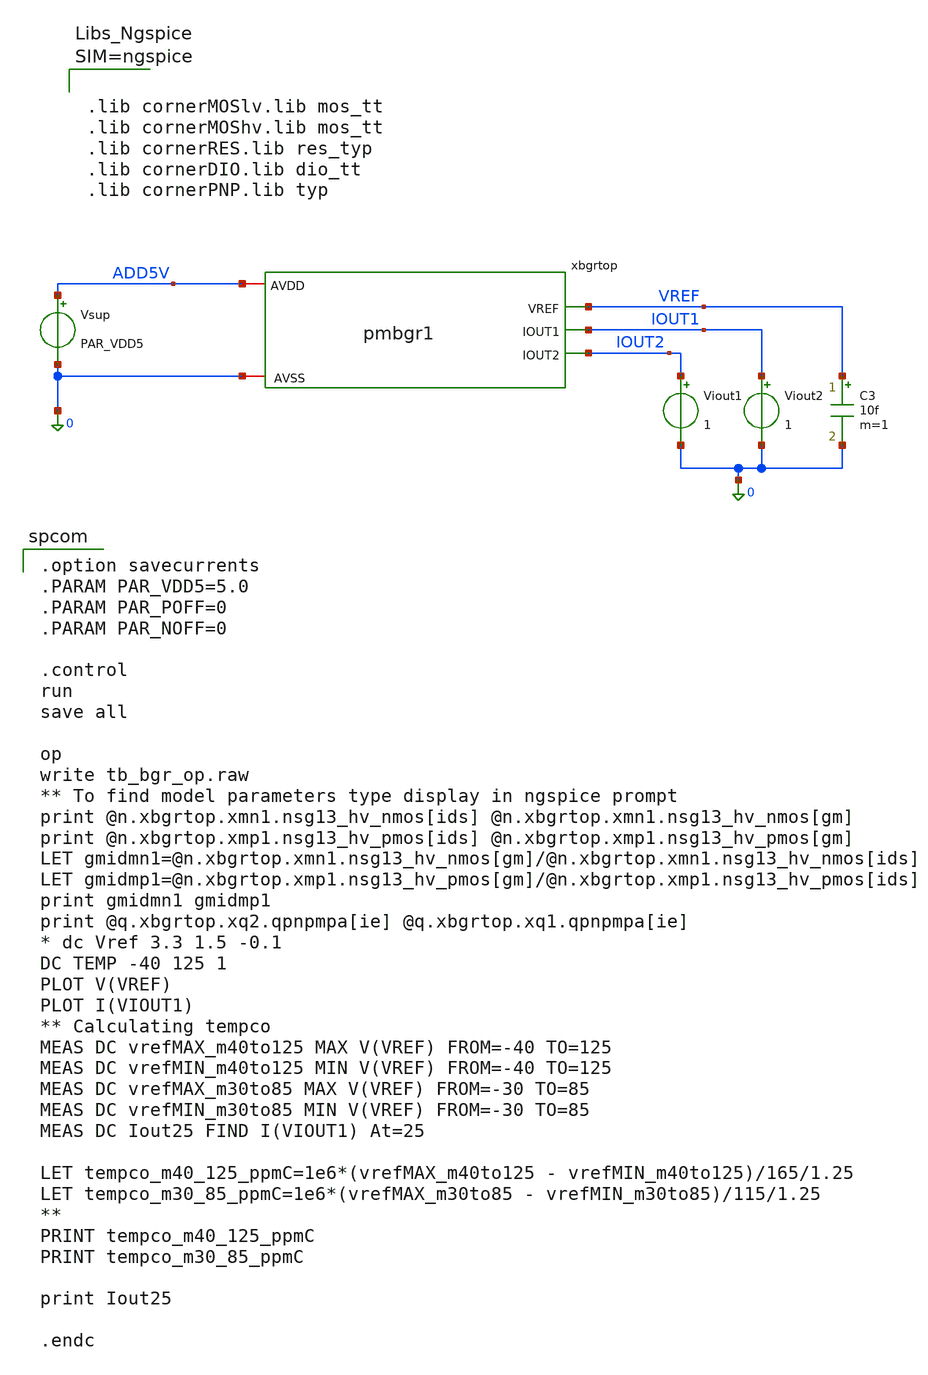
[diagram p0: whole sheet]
** sch_path: xschem/TB_pmbgr1.sch
**.subckt TB_pmbgr1
xbgrtop ADD5V VREF IOUT1 IOUT2 0 pmbgr1
Vsup ADD5V 0 PAR_VDD5
C3 VREF 0 10f m=1
Viout1 IOUT2 0 1
Viout2 IOUT1 0 1
**** begin user architecture code

.option savecurrents
.PARAM PAR_VDD5=5.0
.PARAM PAR_POFF=0
.PARAM PAR_NOFF=0

.control
run
save all

op
write tb_bgr_op.raw
** To find model parameters type display in ngspice prompt
print @n.xbgrtop.xmn1.nsg13_hv_nmos[ids] @n.xbgrtop.xmn1.nsg13_hv_nmos[gm]
print @n.xbgrtop.xmp1.nsg13_hv_pmos[ids] @n.xbgrtop.xmp1.nsg13_hv_pmos[gm]
LET gmidmn1=@n.xbgrtop.xmn1.nsg13_hv_nmos[gm]/@n.xbgrtop.xmn1.nsg13_hv_nmos[ids]
LET gmidmp1=@n.xbgrtop.xmp1.nsg13_hv_pmos[gm]/@n.xbgrtop.xmp1.nsg13_hv_pmos[ids]
print gmidmn1 gmidmp1
print @q.xbgrtop.xq2.qpnpmpa[ie] @q.xbgrtop.xq1.qpnpmpa[ie]
* dc Vref 3.3 1.5 -0.1
DC TEMP -40 125 1
PLOT V(VREF)
PLOT I(VIOUT1)
** Calculating tempco
MEAS DC vrefMAX_m40to125 MAX V(VREF) FROM=-40 TO=125
MEAS DC vrefMIN_m40to125 MIN V(VREF) FROM=-40 TO=125
MEAS DC vrefMAX_m30to85 MAX V(VREF) FROM=-30 TO=85
MEAS DC vrefMIN_m30to85 MIN V(VREF) FROM=-30 TO=85
MEAS DC Iout25 FIND I(VIOUT1) At=25

LET tempco_m40_125_ppmC=1e6*(vrefMAX_m40to125 - vrefMIN_m40to125)/165/1.25
LET tempco_m30_85_ppmC=1e6*(vrefMAX_m30to85 - vrefMIN_m30to85)/115/1.25
**
PRINT tempco_m40_125_ppmC
PRINT tempco_m30_85_ppmC

print Iout25

.endc




.lib cornerMOSlv.lib mos_tt
.lib cornerMOShv.lib mos_tt
.lib cornerRES.lib res_typ
.lib cornerDIO.lib dio_tt
.lib cornerPNP.lib typ



**** end user architecture code
**.ends

* expanding   symbol:  pmbgr1.sym # of pins=5
** sym_path: xschem/pmbgr1.sym
** sch_path: xschem/pmbgr1.sch
.subckt pmbgr1 AVDD VREF IOUT1 IOUT2 AVSS
*.iopin AVDD
*.iopin AVSS
*.opin VREF
*.opin IOUT1
*.opin IOUT2
XQ1 AVSS AVSS Vbe1 pnpMPA a=2p p=6u m=8
XQ2 AVSS AVSS Vbe2 pnpMPA a=2p p=6u m=1
XMN2 Vgn Vgn Vbe2 AVSS sg13_hv_nmos w=2u l=1u ng=1 m=4 mm_ok=1
XMN1 net1 net2 Vbe2_cp AVSS sg13_hv_nmos w=2u l=1u ng=1 m=8 mm_ok=1
XMP2 Vgn Vgp AVDD AVDD sg13_hv_pmos w=1u l=4u ng=1 m=2 mm_ok=1
XMP1 net1 net1 AVDD AVDD sg13_hv_pmos w=1u l=4u ng=1 m=4 mm_ok=1
XR2 Vbe2_cp Vbe1 AVSS rhigh w=1.1u l=25u m=1 b=0 mm_ok=1
XMP3 IOUT1 net1 AVDD AVDD sg13_hv_pmos w=1u l=4u ng=1 m=4 mm_ok=1
XMP4 IOUT2 net1 AVDD AVDD sg13_hv_pmos w=1u l=4u ng=1 m=4 mm_ok=1
XMP5 VREF Vgp AVDD AVDD sg13_hv_pmos w=1u l=4u ng=1 m=2 mm_ok=1
XR1 VREF Vbe2 AVSS rhigh w=1.1u l=351.5u m=1 b=0 mm_ok=1
V1 net2 Vgn PAR_NOFF
V2 net1 Vgp PAR_POFF
.ends

.end
